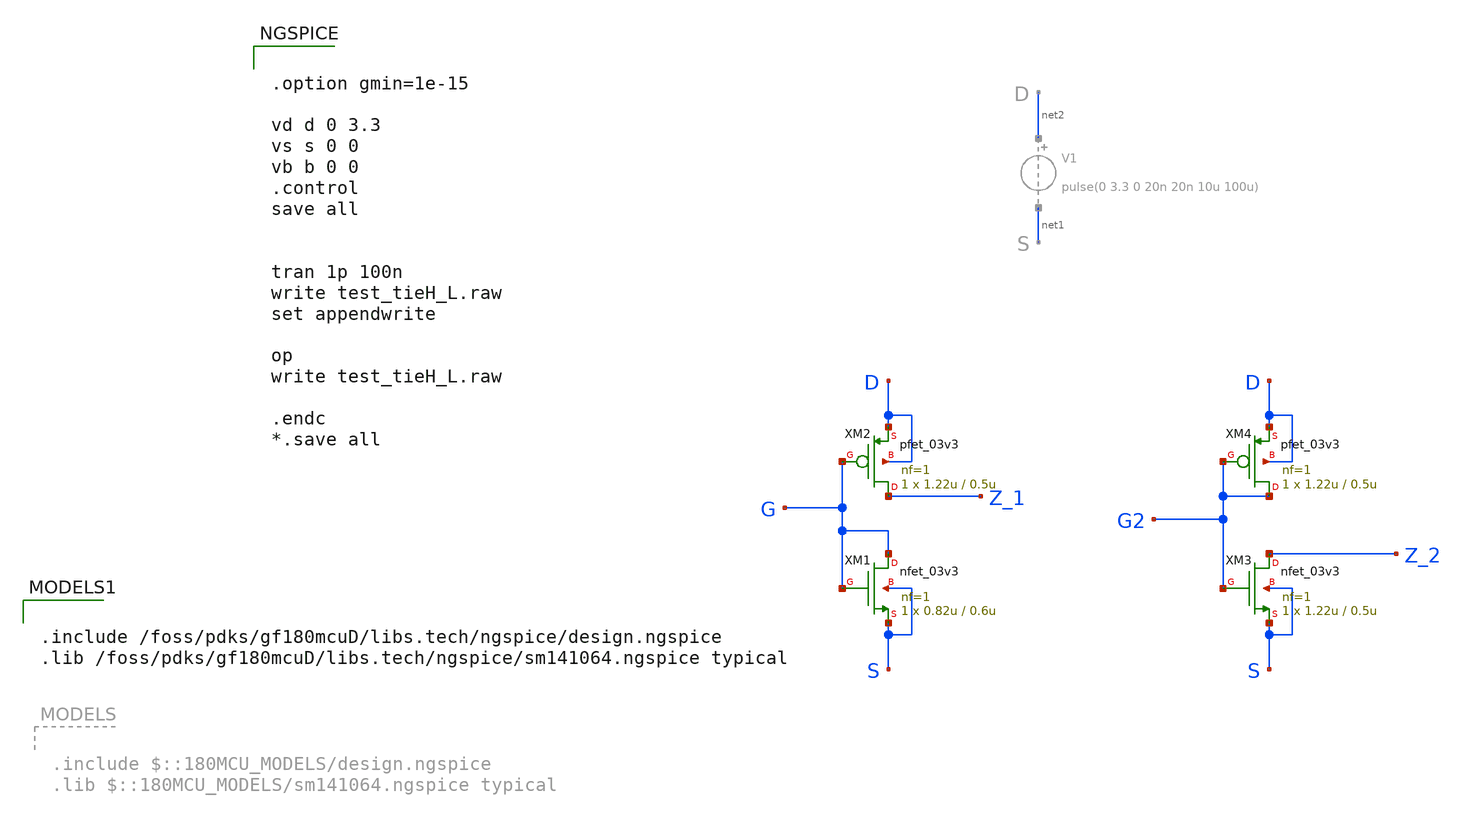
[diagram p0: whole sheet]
** sch_path: integration/padframe/test_tieH_L.sch
**.subckt test_tieH_L
XM1 G G S S nfet_03v3 L=0.6u W=0.82u nf=1 ad='int((nf+1)/2) * W/nf * 0.18u' as='int((nf+2)/2) * W/nf * 0.18u'
+ pd='2*int((nf+1)/2) * (W/nf + 0.18u)' ps='2*int((nf+2)/2) * (W/nf + 0.18u)' nrd='0.18u / W' nrs='0.18u / W'
+ sa=0 sb=0 sd=0 m=1
XM2 Z_1 G D D pfet_03v3 L=0.5u W=1.22u nf=1 ad='int((nf+1)/2) * W/nf * 0.18u' as='int((nf+2)/2) * W/nf * 0.18u'
+ pd='2*int((nf+1)/2) * (W/nf + 0.18u)' ps='2*int((nf+2)/2) * (W/nf + 0.18u)' nrd='0.18u / W' nrs='0.18u / W'
+ sa=0 sb=0 sd=0 m=1
XM3 Z_2 G2 S S nfet_03v3 L=0.5u W=1.22u nf=1 ad='int((nf+1)/2) * W/nf * 0.18u' as='int((nf+2)/2) * W/nf * 0.18u'
+ pd='2*int((nf+1)/2) * (W/nf + 0.18u)' ps='2*int((nf+2)/2) * (W/nf + 0.18u)' nrd='0.18u / W' nrs='0.18u / W'
+ sa=0 sb=0 sd=0 m=1
XM4 G2 G2 D D pfet_03v3 L=0.5u W=1.22u nf=1 ad='int((nf+1)/2) * W/nf * 0.18u' as='int((nf+2)/2) * W/nf * 0.18u'
+ pd='2*int((nf+1)/2) * (W/nf + 0.18u)' ps='2*int((nf+2)/2) * (W/nf + 0.18u)' nrd='0.18u / W' nrs='0.18u / W'
+ sa=0 sb=0 sd=0 m=1
**** begin user architecture code


.option gmin=1e-15

vd d 0 3.3
vs s 0 0
vb b 0 0
.control
save all


tran 1p 100n
write test_tieH_L.raw
set appendwrite

op
write test_tieH_L.raw

.endc
*.save all



.include /foss/pdks/gf180mcuD/libs.tech/ngspice/design.ngspice
.lib /foss/pdks/gf180mcuD/libs.tech/ngspice/sm141064.ngspice typical

**** end user architecture code
**.ends
.end
